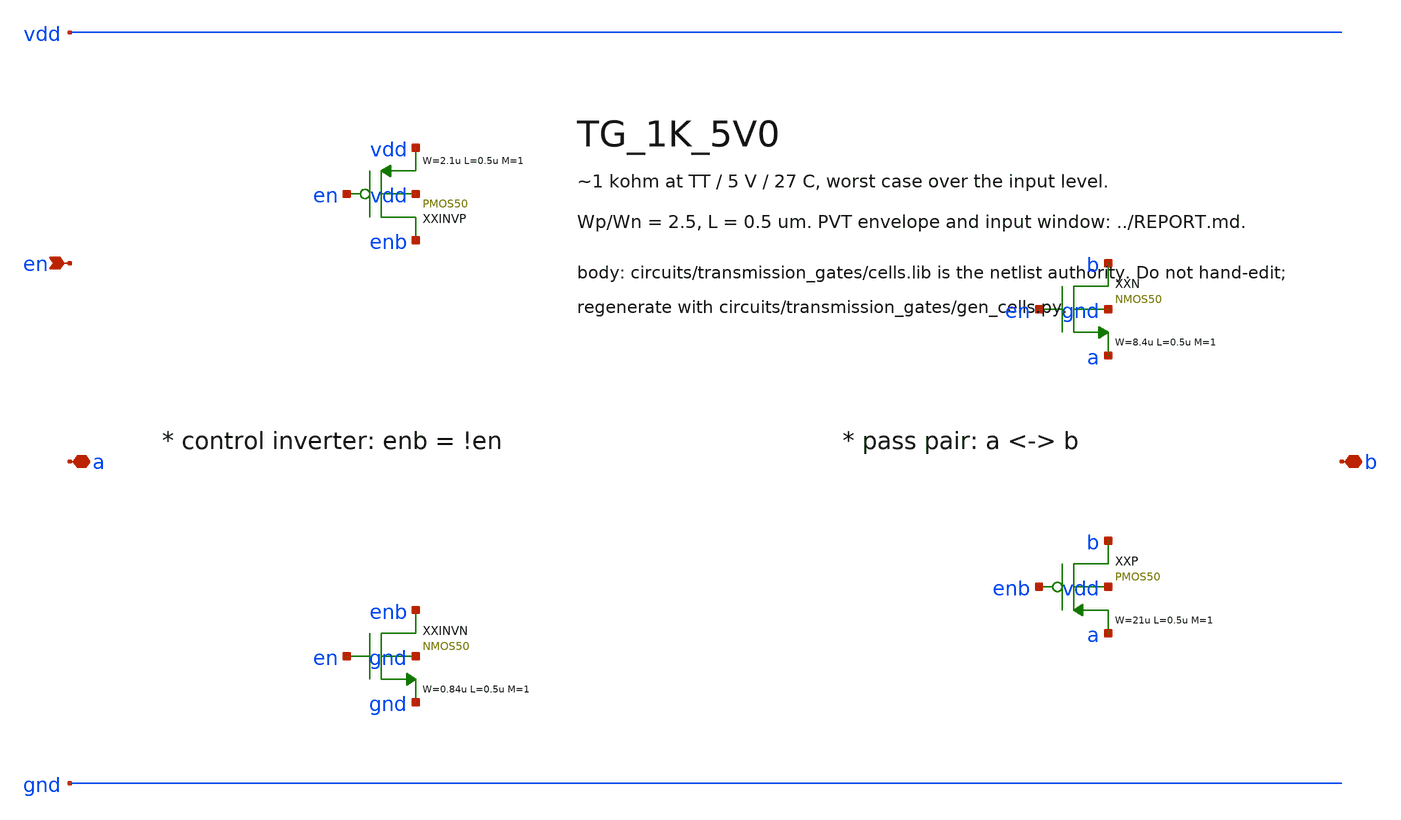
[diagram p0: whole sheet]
** sch_path: xschem/transmission_gates/TG_1K_5V0.sch
**.subckt TG_1K_5V0 a b en
*.iopin a
*.iopin b
*.ipin en
XXINVP enb en vdd vdd PMOS50 W=2.1u L=0.5u M=1 MM_SIGMA=0
XXINVN enb en gnd gnd NMOS50 W=0.84u L=0.5u M=1 MM_SIGMA=0
XXN b en a gnd NMOS50 W=8.4u L=0.5u M=1 MM_SIGMA=0
XXP b enb a vdd PMOS50 W=21u L=0.5u M=1 MM_SIGMA=0
**.ends
.end
